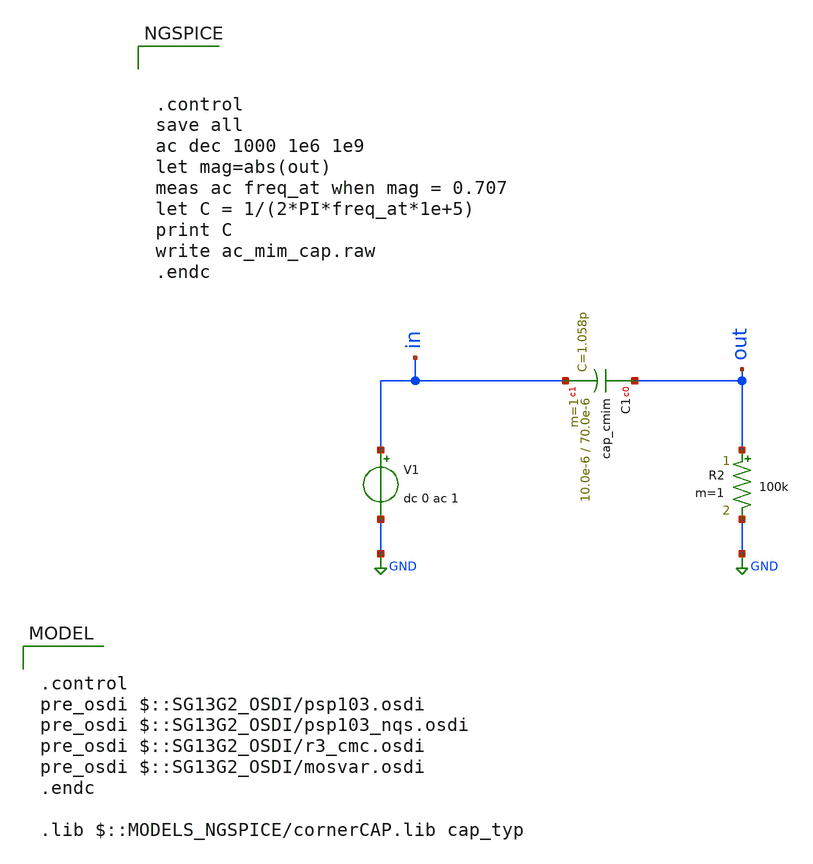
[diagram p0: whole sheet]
** sch_path: ihp-sg13g2/xschem_libs/sg13g2_tests/ac_mim_cap/schematic/ac_mim_cap.sch
* Copyright 2021 Stefan Frederik Schippers
* Licensed under the Apache License, Version 2.0 (the "License");
* you may not use this file except in compliance with the License.
* You may obtain a copy of the License at
* https://www.apache.org/licenses/LICENSE-2.0
* Unless required by applicable law or agreed to in writing, software
* distributed under the License is distributed on an "AS IS" BASIS,
* WITHOUT WARRANTIES OR CONDITIONS OF ANY KIND, either express or implied.
* See the License for the specific language governing permissions and
* limitations under the License.
* Copyright 2023 IHP PDK Authors
**.subckt ac_mim_cap
V1 in GND dc 0 ac 1
R2 out GND 100k m=1
XC1 out in cap_cmim w=10.0e-6 l=70.0e-6 m=1 mm_ok=1
**** begin user architecture code



.control
save all
ac dec 1000 1e6 1e9
let mag=abs(out)
meas ac freq_at when mag = 0.707
let C = 1/(2*PI*freq_at*1e+5)
print C
write ac_mim_cap.raw
.endc



.control
pre_osdi $::SG13G2_OSDI/psp103.osdi
pre_osdi $::SG13G2_OSDI/psp103_nqs.osdi
pre_osdi $::SG13G2_OSDI/r3_cmc.osdi
pre_osdi $::SG13G2_OSDI/mosvar.osdi
.endc

.lib $::MODELS_NGSPICE/cornerCAP.lib cap_typ

**** end user architecture code
**.ends
.GLOBAL GND
.end
